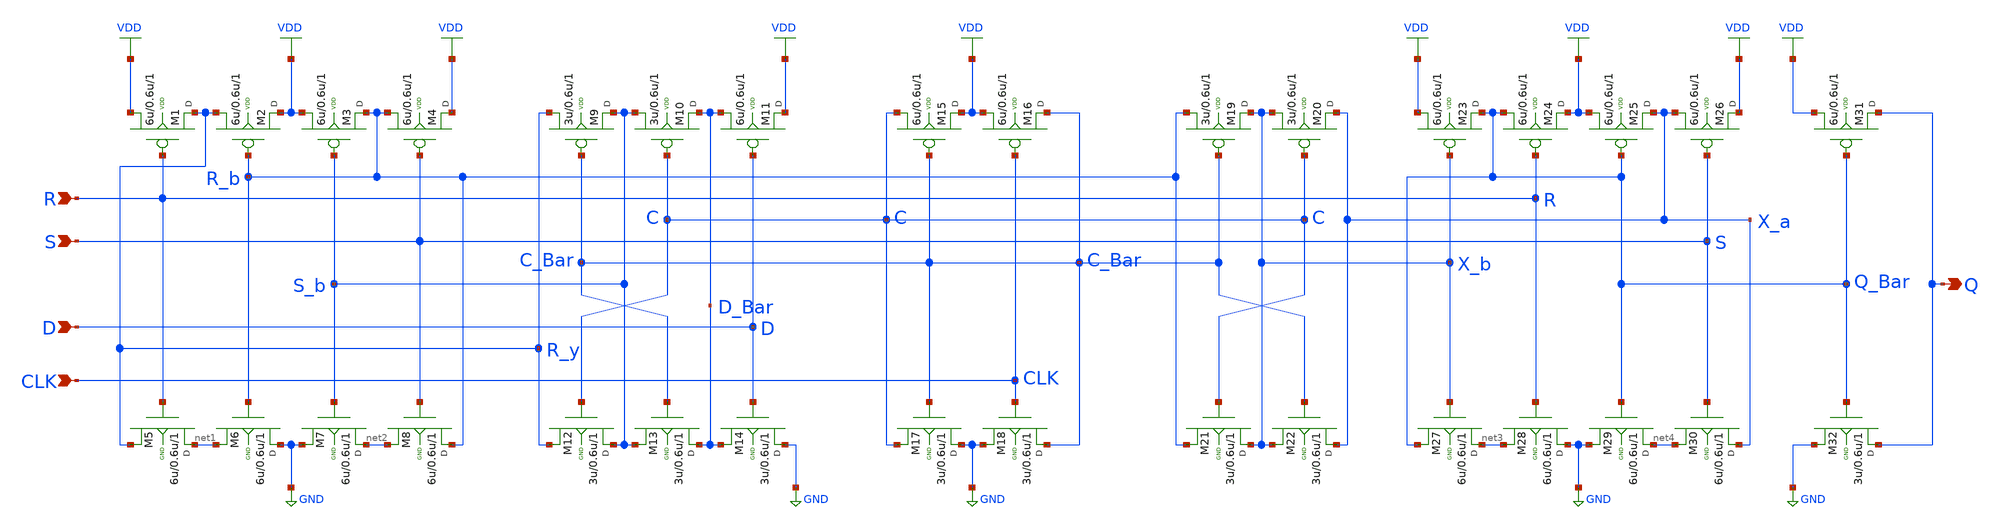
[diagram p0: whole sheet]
** sch_path: sch/DFFSR.sch
**.subckt DFFSR R S D CLK Q
*.ipin R
*.ipin S
*.ipin D
*.ipin CLK
*.opin Q
M1 R_y R VDD VDD pfet w=6u l=0.6u m=1
M2 VDD R_b R_y VDD pfet w=6u l=0.6u m=1
M3 R_b S_b VDD VDD pfet w=6u l=0.6u m=1
M4 VDD S R_b VDD pfet w=6u l=0.6u m=1
M5 net1 R R_y GND nfet w=6u l=0.6u m=1
M6 GND R_b net1 GND nfet w=6u l=0.6u m=1
M7 net2 S_b GND GND nfet w=6u l=0.6u m=1
M8 R_b S net2 GND nfet w=6u l=0.6u m=1
M9 S_b C_Bar R_y VDD pfet w=3u l=0.6u m=1
M10 D_Bar C S_b VDD pfet w=3u l=0.6u m=1
M11 VDD D D_Bar VDD pfet w=6u l=0.6u m=1
M12 S_b C R_y GND nfet w=3u l=0.6u m=1
M13 D_Bar C_Bar S_b GND nfet w=3u l=0.6u m=1
M14 GND D D_Bar GND nfet w=3u l=0.6u m=1
M15 VDD C_Bar C VDD pfet w=6u l=0.6u m=1
M16 C_Bar CLK VDD VDD pfet w=6u l=0.6u m=1
M17 GND C_Bar C GND nfet w=3u l=0.6u m=1
M18 C_Bar CLK GND GND nfet w=3u l=0.6u m=1
M19 X_b C_Bar R_b VDD pfet w=3u l=0.6u m=1
M20 X_a C X_b VDD pfet w=3u l=0.6u m=1
M21 X_b C R_b GND nfet w=3u l=0.6u m=1
M22 X_a C_Bar X_b GND nfet w=3u l=0.6u m=1
M23 Q_Bar X_b VDD VDD pfet w=6u l=0.6u m=1
M24 VDD R Q_Bar VDD pfet w=6u l=0.6u m=1
M25 X_a Q_Bar VDD VDD pfet w=6u l=0.6u m=1
M26 VDD S X_a VDD pfet w=6u l=0.6u m=1
M27 net3 X_b Q_Bar GND nfet w=6u l=0.6u m=1
M28 GND R net3 GND nfet w=6u l=0.6u m=1
M29 net4 Q_Bar GND GND nfet w=6u l=0.6u m=1
M30 X_a S net4 GND nfet w=6u l=0.6u m=1
M31 Q Q_Bar VDD VDD pfet w=6u l=0.6u m=1
M32 Q Q_Bar GND GND nfet w=3u l=0.6u m=1
**.ends
.GLOBAL VDD
.GLOBAL GND
.end
